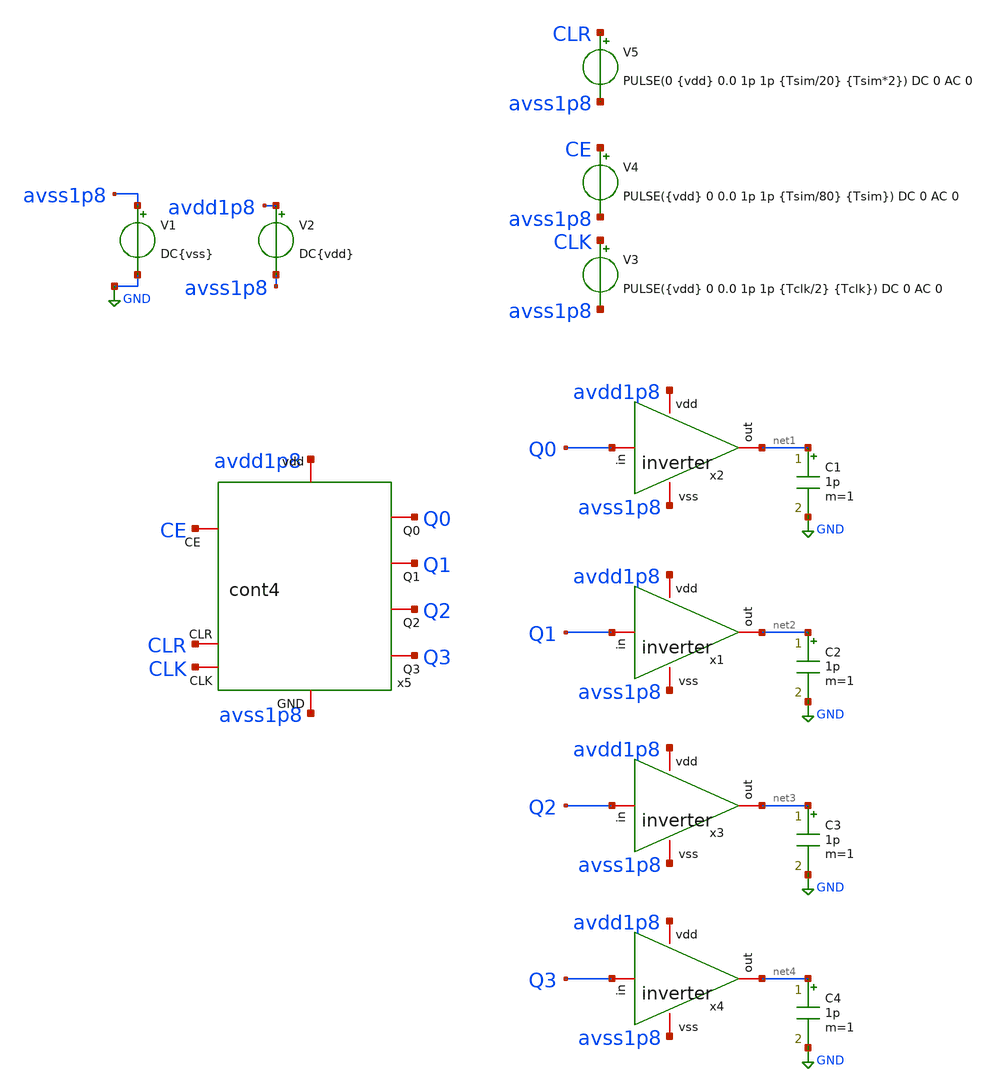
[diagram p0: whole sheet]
** sch_path: simbolos y esquematicos/tb_cont4.sch
**.subckt tb_cont4
V3 CLK avss1p8 PULSE({vdd} 0 0.0 1p 1p {Tclk/2} {Tclk}) DC 0 AC 0
V1 avss1p8 GND DC{vss}
V2 avdd1p8 avss1p8 DC{vdd}
x2 avdd1p8 Q0 net1 avss1p8 inverter
C1 net1 GND 1p m=1
V4 CE avss1p8 PULSE({vdd} 0 0.0 1p 1p {Tsim/80} {Tsim}) DC 0 AC 0
x1 avdd1p8 Q1 net2 avss1p8 inverter
C2 net2 GND 1p m=1
x3 avdd1p8 Q2 net3 avss1p8 inverter
C3 net3 GND 1p m=1
x4 avdd1p8 Q3 net4 avss1p8 inverter
C4 net4 GND 1p m=1
x5 avdd1p8 Q0 CE Q1 Q2 Q3 avss1p8 CLR CLK cont4
V5 CLR avss1p8 PULSE(0 {vdd} 0.0 1p 1p {Tsim/20} {Tsim*2}) DC 0 AC 0
**** begin user architecture code


* Circuit Parameters
.param vdd= 1.8
.param vss= 0.0
.param Tsim= 1u
.param Tclk = 15n
.options TEMP = 65.0
* Include Models
.lib /foss/pdks/sky130A/libs.tech/ngspice/sky130.lib.spice TT
* OP Parameters & Singals to save
.save all
*Simulations
.control
tran 0.01u 1u
setplot tran1
plot v(CE) v(CLR)+2 v(CLK)+4
plot v(CLK) v(Q0)+2 v(Q1)+4 v(Q2)+6 v(Q3)+8 v(CLR)+10
.endc
.end


**** end user architecture code
**.ends
.GLOBAL GND
.end
